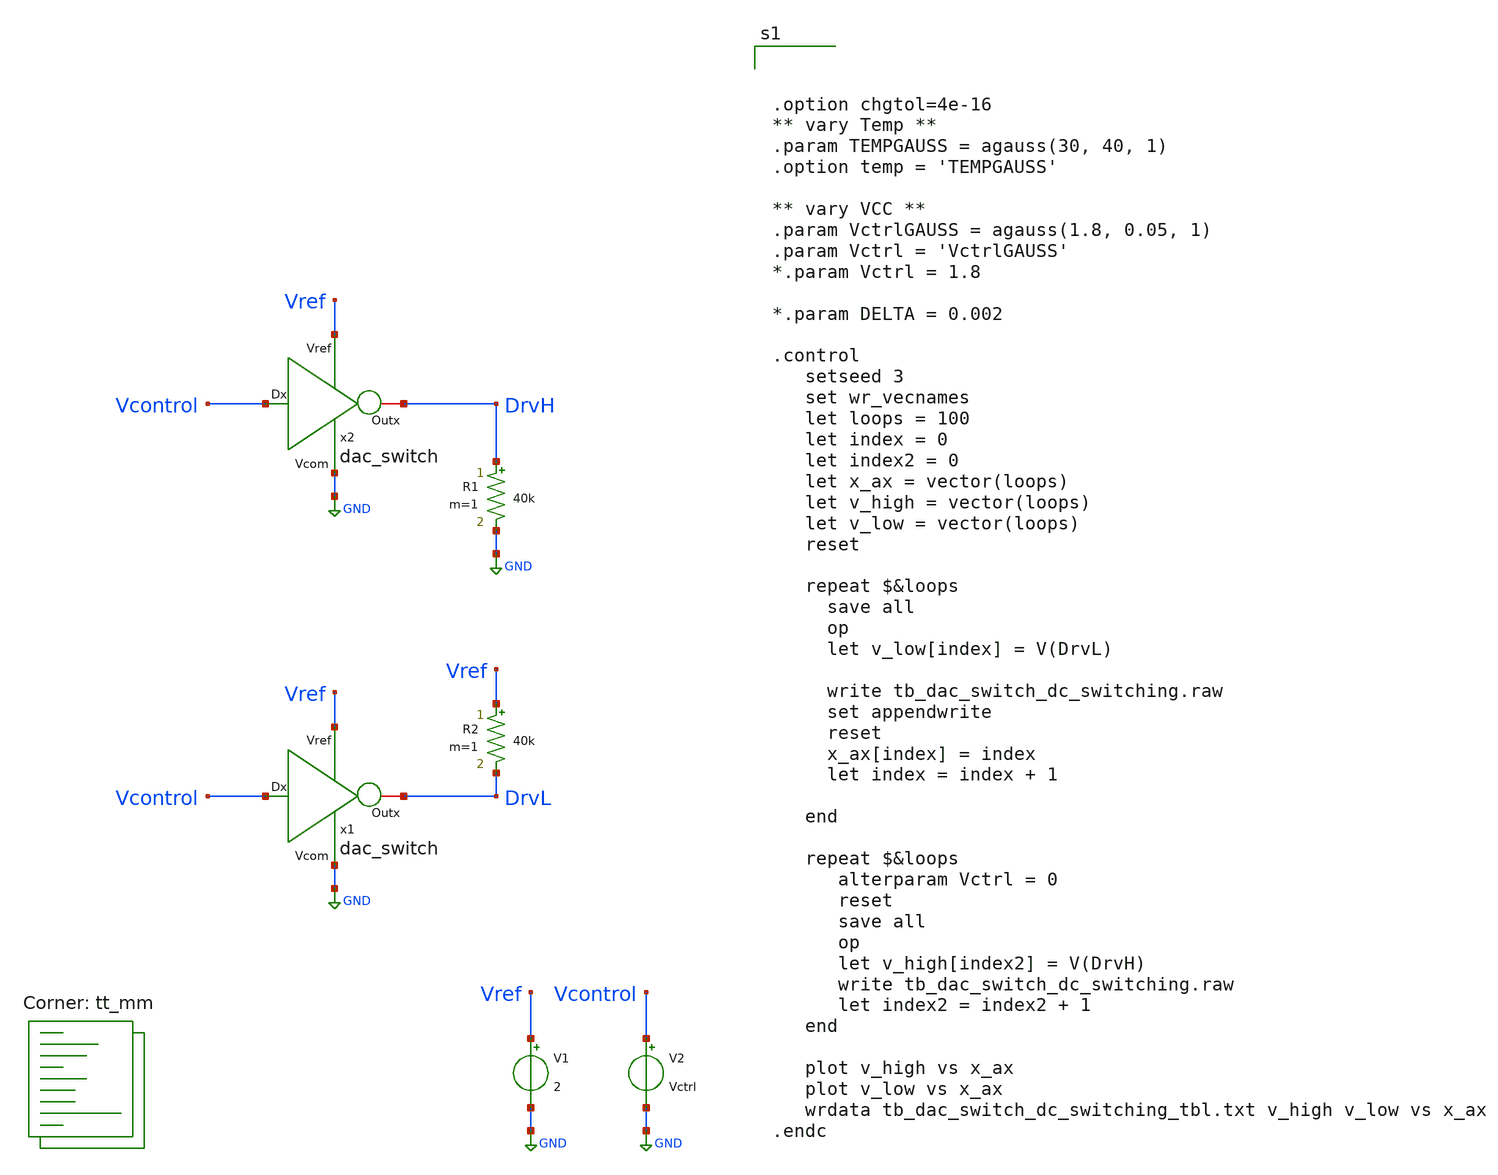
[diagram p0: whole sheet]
** sch_path: xschem/tb_dac_switch_dc_switching.sch
**.subckt tb_dac_switch_dc_switching
V1 Vref GND 2
x1 Vref Vcontrol DrvL GND dac_switch
V2 Vcontrol GND Vctrl
x2 Vref Vcontrol DrvH GND dac_switch
R1 DrvH GND 40k m=1
R2 Vref DrvL 40k m=1
**** begin user architecture code
.lib $::SKYWATER_MODELS/sky130.lib.spice tt_mm



.option chgtol=4e-16
** vary Temp **
.param TEMPGAUSS = agauss(30, 40, 1)
.option temp = 'TEMPGAUSS'

** vary VCC **
.param VctrlGAUSS = agauss(1.8, 0.05, 1)
.param Vctrl = 'VctrlGAUSS'
*.param Vctrl = 1.8

*.param DELTA = 0.002

.control
   setseed 3
   set wr_vecnames
   let loops = 100
   let index = 0
   let index2 = 0
   let x_ax = vector(loops)
   let v_high = vector(loops)
   let v_low = vector(loops)
   reset

   repeat $&loops
     save all
     op
     let v_low[index] = V(DrvL)

     write tb_dac_switch_dc_switching.raw
     set appendwrite
     reset
     x_ax[index] = index
     let index = index + 1

   end

   repeat $&loops
      alterparam Vctrl = 0
      reset
      save all
      op
      let v_high[index2] = V(DrvH)
      write tb_dac_switch_dc_switching.raw
      let index2 = index2 + 1
   end

   plot v_high vs x_ax
   plot v_low vs x_ax
   wrdata tb_dac_switch_dc_switching_tbl.txt v_high v_low vs x_ax
.endc



**** end user architecture code
**.ends

* expanding   symbol:  dac_switch.sym # of pins=4
** sym_path: xschem/dac_switch.sym
** sch_path: xschem/dac_switch.sch
.subckt dac_switch Vref Dx Outx Vcom
*.ipin Dx
*.opin Outx
*.iopin Vref
*.iopin Vcom
XM1 Outx Dx Vref Vref sky130_fd_pr__pfet_g5v0d10v5 L=0.5 W=16 nf=1 ad='int((nf+1)/2) * W/nf * 0.29' as='int((nf+2)/2) * W/nf * 0.29'
+ pd='2*int((nf+1)/2) * (W/nf + 0.29)' ps='2*int((nf+2)/2) * (W/nf + 0.29)' nrd='0.29 / W' nrs='0.29 / W'
+ sa=0 sb=0 sd=0 mult=1 m=1
XM2 Outx Dx Vcom Vcom sky130_fd_pr__nfet_g5v0d10v5 L=0.5 W=7 nf=1 ad='int((nf+1)/2) * W/nf * 0.29' as='int((nf+2)/2) * W/nf * 0.29'
+ pd='2*int((nf+1)/2) * (W/nf + 0.29)' ps='2*int((nf+2)/2) * (W/nf + 0.29)' nrd='0.29 / W' nrs='0.29 / W'
+ sa=0 sb=0 sd=0 mult=1 m=1
.ends

.GLOBAL GND
.end
